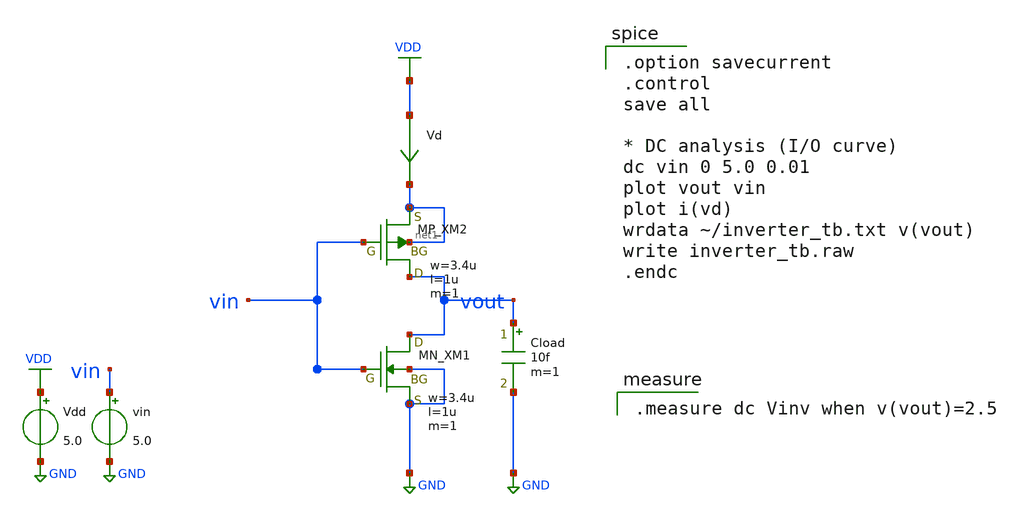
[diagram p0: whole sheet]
** sch_path: member_project/inverter/RISE-A/jijinbei/inverter_sim.sch
**.subckt inverter_sim
XXM1 vout vin GND GND NMOS w=3.4u l=1u nrd=0 nrs=0 m=1
XXM2 vout vin net1 net1 PMOS w=3.4u l=1u nrd=0 nrs=0 m=1
Cload vout GND 10f m=1
vin vin GND 5.0
Vdd VDD GND 5.0
Vd VDD net1 0
.save i(vd)
**** begin user architecture code
 .include $::LIB/ip62_models
 .option savecurrent
.control
save all

* DC analysis (I/O curve)
dc vin 0 5.0 0.01
plot vout vin
plot i(vd)
wrdata ~/inverter_tb.txt v(vout)
write inverter_tb.raw
.endc
 .measure dc Vinv when v(vout)=2.5

**** end user architecture code
**.ends
.GLOBAL VDD
.GLOBAL GND
.end
